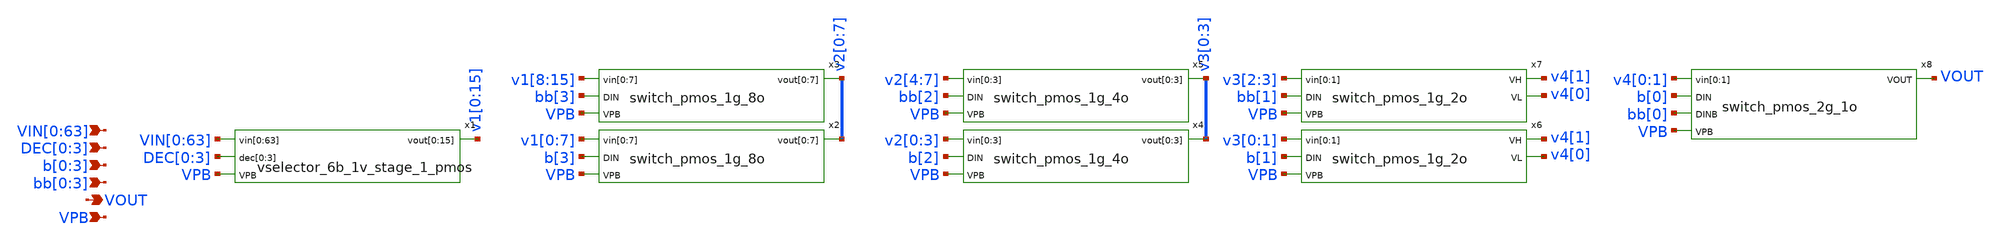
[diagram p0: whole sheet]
** sch_path: xschem/vselector_6b_1v_pmos.sch
**.subckt vselector_6b_1v_pmos
*+ VIN[0],VIN[1],VIN[2],VIN[3],VIN[4],VIN[5],VIN[6],VIN[7],VIN[8],VIN[9],VIN[10],VIN[11],VIN[12],VIN[13],VIN[14],VIN[15],VIN[16],VIN[17],VIN[18],VIN[19],VIN[20],VIN[21],VIN[22],VIN[23],VIN[24],VIN[25],VIN[26],VIN[27],VIN[28],VIN[29],VIN[30],VIN[31],VIN[32],VIN[33],VIN[34],VIN[35],VIN[36],VIN[37],VIN[38],VIN[39],VIN[40],VIN[41],VIN[42],VIN[43],VIN[44],VIN[45],VIN[46],VIN[47],VIN[48],VIN[49],VIN[50],VIN[51],VIN[52],VIN[53],VIN[54],VIN[55],VIN[56],VIN[57],VIN[58],VIN[59],VIN[60],VIN[61],VIN[62],VIN[63] VOUT VPB DEC[0],DEC[1],DEC[2],DEC[3] b[0],b[1],b[2],b[3] bb[0],bb[1],bb[2],bb[3]
*.ipin
*+ VIN[0],VIN[1],VIN[2],VIN[3],VIN[4],VIN[5],VIN[6],VIN[7],VIN[8],VIN[9],VIN[10],VIN[11],VIN[12],VIN[13],VIN[14],VIN[15],VIN[16],VIN[17],VIN[18],VIN[19],VIN[20],VIN[21],VIN[22],VIN[23],VIN[24],VIN[25],VIN[26],VIN[27],VIN[28],VIN[29],VIN[30],VIN[31],VIN[32],VIN[33],VIN[34],VIN[35],VIN[36],VIN[37],VIN[38],VIN[39],VIN[40],VIN[41],VIN[42],VIN[43],VIN[44],VIN[45],VIN[46],VIN[47],VIN[48],VIN[49],VIN[50],VIN[51],VIN[52],VIN[53],VIN[54],VIN[55],VIN[56],VIN[57],VIN[58],VIN[59],VIN[60],VIN[61],VIN[62],VIN[63]
*.opin VOUT
*.ipin VPB
*.ipin DEC[0],DEC[1],DEC[2],DEC[3]
*.ipin b[0],b[1],b[2],b[3]
*.ipin bb[0],bb[1],bb[2],bb[3]
x1 VIN[0] VIN[1] VIN[2] VIN[3] VIN[4] VIN[5] VIN[6] VIN[7] VIN[8] VIN[9] VIN[10] VIN[11] VIN[12]
+ VIN[13] VIN[14] VIN[15] VIN[16] VIN[17] VIN[18] VIN[19] VIN[20] VIN[21] VIN[22] VIN[23] VIN[24] VIN[25]
+ VIN[26] VIN[27] VIN[28] VIN[29] VIN[30] VIN[31] VIN[32] VIN[33] VIN[34] VIN[35] VIN[36] VIN[37] VIN[38]
+ VIN[39] VIN[40] VIN[41] VIN[42] VIN[43] VIN[44] VIN[45] VIN[46] VIN[47] VIN[48] VIN[49] VIN[50] VIN[51]
+ VIN[52] VIN[53] VIN[54] VIN[55] VIN[56] VIN[57] VIN[58] VIN[59] VIN[60] VIN[61] VIN[62] VIN[63] DEC[0]
+ DEC[1] DEC[2] DEC[3] v1[0] v1[1] v1[2] v1[3] v1[4] v1[5] v1[6] v1[7] v1[8] v1[9] v1[10] v1[11] v1[12]
+ v1[13] v1[14] v1[15] VPB vselector_6b_1v_stage_1_pmos
x2 v1[0] v1[1] v1[2] v1[3] v1[4] v1[5] v1[6] v1[7] b[3] v2[0] v2[1] v2[2] v2[3] v2[4] v2[5] v2[6]
+ v2[7] VPB switch_pmos_1g_8o
x3 v1[8] v1[9] v1[10] v1[11] v1[12] v1[13] v1[14] v1[15] bb[3] v2[0] v2[1] v2[2] v2[3] v2[4] v2[5]
+ v2[6] v2[7] VPB switch_pmos_1g_8o
x4 v2[0] v2[1] v2[2] v2[3] b[2] v3[0] v3[1] v3[2] v3[3] VPB switch_pmos_1g_4o
x5 v2[4] v2[5] v2[6] v2[7] bb[2] v3[0] v3[1] v3[2] v3[3] VPB switch_pmos_1g_4o
x6 v3[0] v3[1] b[1] v4[1] v4[0] VPB switch_pmos_1g_2o
x7 v3[2] v3[3] bb[1] v4[1] v4[0] VPB switch_pmos_1g_2o
x8 v4[0] v4[1] b[0] bb[0] VOUT VPB switch_pmos_2g_1o
**.ends

* expanding   symbol:  vselector_6b_1v_stage_1_pmos.sym # of pins=4
** sym_path: xschem/vselector_6b_1v_stage_1_pmos.sym
** sch_path: xschem/vselector_6b_1v_stage_1_pmos.sch
.subckt vselector_6b_1v_stage_1_pmos vin[0] vin[1] vin[2] vin[3] vin[4] vin[5] vin[6] vin[7] vin[8]
+ vin[9] vin[10] vin[11] vin[12] vin[13] vin[14] vin[15] vin[16] vin[17] vin[18] vin[19] vin[20] vin[21]
+ vin[22] vin[23] vin[24] vin[25] vin[26] vin[27] vin[28] vin[29] vin[30] vin[31] vin[32] vin[33] vin[34]
+ vin[35] vin[36] vin[37] vin[38] vin[39] vin[40] vin[41] vin[42] vin[43] vin[44] vin[45] vin[46] vin[47]
+ vin[48] vin[49] vin[50] vin[51] vin[52] vin[53] vin[54] vin[55] vin[56] vin[57] vin[58] vin[59] vin[60]
+ vin[61] vin[62] vin[63] dec[0] dec[1] dec[2] dec[3] vout[0] vout[1] vout[2] vout[3] vout[4] vout[5] vout[6]
+ vout[7] vout[8] vout[9] vout[10] vout[11] vout[12] vout[13] vout[14] vout[15] VPB
*.ipin
*+ vin[0],vin[1],vin[2],vin[3],vin[4],vin[5],vin[6],vin[7],vin[8],vin[9],vin[10],vin[11],vin[12],vin[13],vin[14],vin[15],vin[16],vin[17],vin[18],vin[19],vin[20],vin[21],vin[22],vin[23],vin[24],vin[25],vin[26],vin[27],vin[28],vin[29],vin[30],vin[31],vin[32],vin[33],vin[34],vin[35],vin[36],vin[37],vin[38],vin[39],vin[40],vin[41],vin[42],vin[43],vin[44],vin[45],vin[46],vin[47],vin[48],vin[49],vin[50],vin[51],vin[52],vin[53],vin[54],vin[55],vin[56],vin[57],vin[58],vin[59],vin[60],vin[61],vin[62],vin[63]
*.opin
*+ vout[0],vout[1],vout[2],vout[3],vout[4],vout[5],vout[6],vout[7],vout[8],vout[9],vout[10],vout[11],vout[12],vout[13],vout[14],vout[15]
*.ipin VPB
*.ipin dec[0],dec[1],dec[2],dec[3]
x1 vin[0] vin[1] vin[2] vin[3] vin[4] vin[5] vin[6] vin[7] vin[8] vin[9] vin[10] vin[11] vin[12]
+ vin[13] vin[14] vin[15] dec[0] vout[0] vout[1] vout[2] vout[3] vout[4] vout[5] vout[6] vout[7] vout[8]
+ vout[9] vout[10] vout[11] vout[12] vout[13] vout[14] vout[15] VPB vselector_16b_1v_pmos
x2 vin[16] vin[17] vin[18] vin[19] vin[20] vin[21] vin[22] vin[23] vin[24] vin[25] vin[26] vin[27]
+ vin[28] vin[29] vin[30] vin[31] dec[1] vout[0] vout[1] vout[2] vout[3] vout[4] vout[5] vout[6] vout[7]
+ vout[8] vout[9] vout[10] vout[11] vout[12] vout[13] vout[14] vout[15] VPB vselector_16b_1v_pmos
x3 vin[32] vin[33] vin[34] vin[35] vin[36] vin[37] vin[38] vin[39] vin[40] vin[41] vin[42] vin[43]
+ vin[44] vin[45] vin[46] vin[47] dec[2] vout[0] vout[1] vout[2] vout[3] vout[4] vout[5] vout[6] vout[7]
+ vout[8] vout[9] vout[10] vout[11] vout[12] vout[13] vout[14] vout[15] VPB vselector_16b_1v_pmos
x4 vin[48] vin[49] vin[50] vin[51] vin[52] vin[53] vin[54] vin[55] vin[56] vin[57] vin[58] vin[59]
+ vin[60] vin[61] vin[62] vin[63] dec[3] vout[0] vout[1] vout[2] vout[3] vout[4] vout[5] vout[6] vout[7]
+ vout[8] vout[9] vout[10] vout[11] vout[12] vout[13] vout[14] vout[15] VPB vselector_16b_1v_pmos
.ends


* expanding   symbol:  switch_pmos_1g_8o.sym # of pins=4
** sym_path: xschem/switch_pmos_1g_8o.sym
** sch_path: xschem/switch_pmos_1g_8o.sch
.subckt switch_pmos_1g_8o vin[0] vin[1] vin[2] vin[3] vin[4] vin[5] vin[6] vin[7] DIN vout[0]
+ vout[1] vout[2] vout[3] vout[4] vout[5] vout[6] vout[7] VPB
*.ipin vin[0],vin[1],vin[2],vin[3],vin[4],vin[5],vin[6],vin[7]
*.opin vout[0],vout[1],vout[2],vout[3],vout[4],vout[5],vout[6],vout[7]
*.ipin VPB
*.ipin DIN
.param wp=0.42 wn=0.42 l=0.5

XM1 vout[0] DIN vin[0] VPB sky130_fd_pr__pfet_g5v0d10v5 L=l W=wp nf=1 ad='int((nf+1)/2) * W/nf * 0.29'
+ as='int((nf+2)/2) * W/nf * 0.29' pd='2*int((nf+1)/2) * (W/nf + 0.29)' ps='2*int((nf+2)/2) * (W/nf + 0.29)'
+ nrd='0.29 / W' nrs='0.29 / W' sa=0 sb=0 sd=0 mult=1 m=1
XM2 vout[1] DIN vin[1] VPB sky130_fd_pr__pfet_g5v0d10v5 L=l W=wp nf=1 ad='int((nf+1)/2) * W/nf * 0.29'
+ as='int((nf+2)/2) * W/nf * 0.29' pd='2*int((nf+1)/2) * (W/nf + 0.29)' ps='2*int((nf+2)/2) * (W/nf + 0.29)'
+ nrd='0.29 / W' nrs='0.29 / W' sa=0 sb=0 sd=0 mult=1 m=1
XM3 vout[2] DIN vin[2] VPB sky130_fd_pr__pfet_g5v0d10v5 L=l W=wp nf=1 ad='int((nf+1)/2) * W/nf * 0.29'
+ as='int((nf+2)/2) * W/nf * 0.29' pd='2*int((nf+1)/2) * (W/nf + 0.29)' ps='2*int((nf+2)/2) * (W/nf + 0.29)'
+ nrd='0.29 / W' nrs='0.29 / W' sa=0 sb=0 sd=0 mult=1 m=1
XM4 vout[3] DIN vin[3] VPB sky130_fd_pr__pfet_g5v0d10v5 L=l W=wp nf=1 ad='int((nf+1)/2) * W/nf * 0.29'
+ as='int((nf+2)/2) * W/nf * 0.29' pd='2*int((nf+1)/2) * (W/nf + 0.29)' ps='2*int((nf+2)/2) * (W/nf + 0.29)'
+ nrd='0.29 / W' nrs='0.29 / W' sa=0 sb=0 sd=0 mult=1 m=1
XM5 vout[4] DIN vin[4] VPB sky130_fd_pr__pfet_g5v0d10v5 L=l W=wp nf=1 ad='int((nf+1)/2) * W/nf * 0.29'
+ as='int((nf+2)/2) * W/nf * 0.29' pd='2*int((nf+1)/2) * (W/nf + 0.29)' ps='2*int((nf+2)/2) * (W/nf + 0.29)'
+ nrd='0.29 / W' nrs='0.29 / W' sa=0 sb=0 sd=0 mult=1 m=1
XM6 vout[5] DIN vin[5] VPB sky130_fd_pr__pfet_g5v0d10v5 L=l W=wp nf=1 ad='int((nf+1)/2) * W/nf * 0.29'
+ as='int((nf+2)/2) * W/nf * 0.29' pd='2*int((nf+1)/2) * (W/nf + 0.29)' ps='2*int((nf+2)/2) * (W/nf + 0.29)'
+ nrd='0.29 / W' nrs='0.29 / W' sa=0 sb=0 sd=0 mult=1 m=1
XM7 vout[6] DIN vin[6] VPB sky130_fd_pr__pfet_g5v0d10v5 L=l W=wp nf=1 ad='int((nf+1)/2) * W/nf * 0.29'
+ as='int((nf+2)/2) * W/nf * 0.29' pd='2*int((nf+1)/2) * (W/nf + 0.29)' ps='2*int((nf+2)/2) * (W/nf + 0.29)'
+ nrd='0.29 / W' nrs='0.29 / W' sa=0 sb=0 sd=0 mult=1 m=1
XM8 vout[7] DIN vin[7] VPB sky130_fd_pr__pfet_g5v0d10v5 L=l W=wp nf=1 ad='int((nf+1)/2) * W/nf * 0.29'
+ as='int((nf+2)/2) * W/nf * 0.29' pd='2*int((nf+1)/2) * (W/nf + 0.29)' ps='2*int((nf+2)/2) * (W/nf + 0.29)'
+ nrd='0.29 / W' nrs='0.29 / W' sa=0 sb=0 sd=0 mult=1 m=1
.ends


* expanding   symbol:  switch_pmos_1g_4o.sym # of pins=4
** sym_path: xschem/switch_pmos_1g_4o.sym
** sch_path: xschem/switch_pmos_1g_4o.sch
.subckt switch_pmos_1g_4o vin[0] vin[1] vin[2] vin[3] DIN vout[0] vout[1] vout[2] vout[3] VPB
*.ipin vin[0],vin[1],vin[2],vin[3]
*.opin vout[0],vout[1],vout[2],vout[3]
*.ipin VPB
*.ipin DIN
.param wp=0.42 wn=0.42 l=0.5

XM1 vout[0] DIN vin[0] VPB sky130_fd_pr__pfet_g5v0d10v5 L=l W=wp nf=1 ad='int((nf+1)/2) * W/nf * 0.29'
+ as='int((nf+2)/2) * W/nf * 0.29' pd='2*int((nf+1)/2) * (W/nf + 0.29)' ps='2*int((nf+2)/2) * (W/nf + 0.29)'
+ nrd='0.29 / W' nrs='0.29 / W' sa=0 sb=0 sd=0 mult=1 m=1
XM2 vout[1] DIN vin[1] VPB sky130_fd_pr__pfet_g5v0d10v5 L=l W=wp nf=1 ad='int((nf+1)/2) * W/nf * 0.29'
+ as='int((nf+2)/2) * W/nf * 0.29' pd='2*int((nf+1)/2) * (W/nf + 0.29)' ps='2*int((nf+2)/2) * (W/nf + 0.29)'
+ nrd='0.29 / W' nrs='0.29 / W' sa=0 sb=0 sd=0 mult=1 m=1
XM3 vout[2] DIN vin[2] VPB sky130_fd_pr__pfet_g5v0d10v5 L=l W=wp nf=1 ad='int((nf+1)/2) * W/nf * 0.29'
+ as='int((nf+2)/2) * W/nf * 0.29' pd='2*int((nf+1)/2) * (W/nf + 0.29)' ps='2*int((nf+2)/2) * (W/nf + 0.29)'
+ nrd='0.29 / W' nrs='0.29 / W' sa=0 sb=0 sd=0 mult=1 m=1
XM4 vout[3] DIN vin[3] VPB sky130_fd_pr__pfet_g5v0d10v5 L=l W=wp nf=1 ad='int((nf+1)/2) * W/nf * 0.29'
+ as='int((nf+2)/2) * W/nf * 0.29' pd='2*int((nf+1)/2) * (W/nf + 0.29)' ps='2*int((nf+2)/2) * (W/nf + 0.29)'
+ nrd='0.29 / W' nrs='0.29 / W' sa=0 sb=0 sd=0 mult=1 m=1
.ends


* expanding   symbol:  switch_pmos_1g_2o.sym # of pins=5
** sym_path: xschem/switch_pmos_1g_2o.sym
** sch_path: xschem/switch_pmos_1g_2o.sch
.subckt switch_pmos_1g_2o vin[0] vin[1] DIN VH VL VPB
*.ipin vin[0],vin[1]
*.opin VH
*.ipin VPB
*.ipin DIN
*.opin VL
.param wp=0.42 wn=0.42 l=0.5

XM1 VL DIN vin[0] VPB sky130_fd_pr__pfet_g5v0d10v5 L=l W=wp nf=1 ad='int((nf+1)/2) * W/nf * 0.29' as='int((nf+2)/2) * W/nf * 0.29'
+ pd='2*int((nf+1)/2) * (W/nf + 0.29)' ps='2*int((nf+2)/2) * (W/nf + 0.29)' nrd='0.29 / W' nrs='0.29 / W'
+ sa=0 sb=0 sd=0 mult=1 m=1
XM2 VH DIN vin[1] VPB sky130_fd_pr__pfet_g5v0d10v5 L=l W=wp nf=1 ad='int((nf+1)/2) * W/nf * 0.29' as='int((nf+2)/2) * W/nf * 0.29'
+ pd='2*int((nf+1)/2) * (W/nf + 0.29)' ps='2*int((nf+2)/2) * (W/nf + 0.29)' nrd='0.29 / W' nrs='0.29 / W'
+ sa=0 sb=0 sd=0 mult=1 m=1
.ends


* expanding   symbol:  switch_pmos_2g_1o.sym # of pins=5
** sym_path: xschem/switch_pmos_2g_1o.sym
** sch_path: xschem/switch_pmos_2g_1o.sch
.subckt switch_pmos_2g_1o vin[0] vin[1] DIN DINB VOUT VPB
*.ipin vin[0],vin[1]
*.opin VOUT
*.ipin VPB
*.ipin DIN
*.ipin DINB
.param wp=0.42 wn=0.42 l=0.5

XM1 VOUT DIN vin[0] VPB sky130_fd_pr__pfet_g5v0d10v5 L=l W=wp nf=1 ad='int((nf+1)/2) * W/nf * 0.29' as='int((nf+2)/2) * W/nf * 0.29'
+ pd='2*int((nf+1)/2) * (W/nf + 0.29)' ps='2*int((nf+2)/2) * (W/nf + 0.29)' nrd='0.29 / W' nrs='0.29 / W'
+ sa=0 sb=0 sd=0 mult=1 m=1
XM2 VOUT DINB vin[1] VPB sky130_fd_pr__pfet_g5v0d10v5 L=l W=wp nf=1 ad='int((nf+1)/2) * W/nf * 0.29'
+ as='int((nf+2)/2) * W/nf * 0.29' pd='2*int((nf+1)/2) * (W/nf + 0.29)' ps='2*int((nf+2)/2) * (W/nf + 0.29)'
+ nrd='0.29 / W' nrs='0.29 / W' sa=0 sb=0 sd=0 mult=1 m=1
.ends


* expanding   symbol:  vselector_16b_1v_pmos.sym # of pins=4
** sym_path: xschem/vselector_16b_1v_pmos.sym
** sch_path: xschem/vselector_16b_1v_pmos.sch
.subckt vselector_16b_1v_pmos vin[0] vin[1] vin[2] vin[3] vin[4] vin[5] vin[6] vin[7] vin[8] vin[9]
+ vin[10] vin[11] vin[12] vin[13] vin[14] vin[15] DIN vout[0] vout[1] vout[2] vout[3] vout[4] vout[5] vout[6]
+ vout[7] vout[8] vout[9] vout[10] vout[11] vout[12] vout[13] vout[14] vout[15] VPB
*.ipin
*+ vin[0],vin[1],vin[2],vin[3],vin[4],vin[5],vin[6],vin[7],vin[8],vin[9],vin[10],vin[11],vin[12],vin[13],vin[14],vin[15]
*.opin
*+ vout[0],vout[1],vout[2],vout[3],vout[4],vout[5],vout[6],vout[7],vout[8],vout[9],vout[10],vout[11],vout[12],vout[13],vout[14],vout[15]
*.ipin VPB
*.ipin DIN
.param wp=0.42 wn=0.42 l=0.5

XM1 vout[0] DIN vin[0] VPB sky130_fd_pr__pfet_g5v0d10v5 L=l W=wp nf=1 ad='int((nf+1)/2) * W/nf * 0.29'
+ as='int((nf+2)/2) * W/nf * 0.29' pd='2*int((nf+1)/2) * (W/nf + 0.29)' ps='2*int((nf+2)/2) * (W/nf + 0.29)'
+ nrd='0.29 / W' nrs='0.29 / W' sa=0 sb=0 sd=0 mult=1 m=1
XM2 vout[1] DIN vin[1] VPB sky130_fd_pr__pfet_g5v0d10v5 L=l W=wp nf=1 ad='int((nf+1)/2) * W/nf * 0.29'
+ as='int((nf+2)/2) * W/nf * 0.29' pd='2*int((nf+1)/2) * (W/nf + 0.29)' ps='2*int((nf+2)/2) * (W/nf + 0.29)'
+ nrd='0.29 / W' nrs='0.29 / W' sa=0 sb=0 sd=0 mult=1 m=1
XM3 vout[2] DIN vin[2] VPB sky130_fd_pr__pfet_g5v0d10v5 L=l W=wp nf=1 ad='int((nf+1)/2) * W/nf * 0.29'
+ as='int((nf+2)/2) * W/nf * 0.29' pd='2*int((nf+1)/2) * (W/nf + 0.29)' ps='2*int((nf+2)/2) * (W/nf + 0.29)'
+ nrd='0.29 / W' nrs='0.29 / W' sa=0 sb=0 sd=0 mult=1 m=1
XM4 vout[3] DIN vin[3] VPB sky130_fd_pr__pfet_g5v0d10v5 L=l W=wp nf=1 ad='int((nf+1)/2) * W/nf * 0.29'
+ as='int((nf+2)/2) * W/nf * 0.29' pd='2*int((nf+1)/2) * (W/nf + 0.29)' ps='2*int((nf+2)/2) * (W/nf + 0.29)'
+ nrd='0.29 / W' nrs='0.29 / W' sa=0 sb=0 sd=0 mult=1 m=1
XM5 vout[4] DIN vin[4] VPB sky130_fd_pr__pfet_g5v0d10v5 L=l W=wp nf=1 ad='int((nf+1)/2) * W/nf * 0.29'
+ as='int((nf+2)/2) * W/nf * 0.29' pd='2*int((nf+1)/2) * (W/nf + 0.29)' ps='2*int((nf+2)/2) * (W/nf + 0.29)'
+ nrd='0.29 / W' nrs='0.29 / W' sa=0 sb=0 sd=0 mult=1 m=1
XM6 vout[5] DIN vin[5] VPB sky130_fd_pr__pfet_g5v0d10v5 L=l W=wp nf=1 ad='int((nf+1)/2) * W/nf * 0.29'
+ as='int((nf+2)/2) * W/nf * 0.29' pd='2*int((nf+1)/2) * (W/nf + 0.29)' ps='2*int((nf+2)/2) * (W/nf + 0.29)'
+ nrd='0.29 / W' nrs='0.29 / W' sa=0 sb=0 sd=0 mult=1 m=1
XM7 vout[6] DIN vin[6] VPB sky130_fd_pr__pfet_g5v0d10v5 L=l W=wp nf=1 ad='int((nf+1)/2) * W/nf * 0.29'
+ as='int((nf+2)/2) * W/nf * 0.29' pd='2*int((nf+1)/2) * (W/nf + 0.29)' ps='2*int((nf+2)/2) * (W/nf + 0.29)'
+ nrd='0.29 / W' nrs='0.29 / W' sa=0 sb=0 sd=0 mult=1 m=1
XM8 vout[7] DIN vin[7] VPB sky130_fd_pr__pfet_g5v0d10v5 L=l W=wp nf=1 ad='int((nf+1)/2) * W/nf * 0.29'
+ as='int((nf+2)/2) * W/nf * 0.29' pd='2*int((nf+1)/2) * (W/nf + 0.29)' ps='2*int((nf+2)/2) * (W/nf + 0.29)'
+ nrd='0.29 / W' nrs='0.29 / W' sa=0 sb=0 sd=0 mult=1 m=1
XM9 vout[8] DIN vin[8] VPB sky130_fd_pr__pfet_g5v0d10v5 L=l W=wp nf=1 ad='int((nf+1)/2) * W/nf * 0.29'
+ as='int((nf+2)/2) * W/nf * 0.29' pd='2*int((nf+1)/2) * (W/nf + 0.29)' ps='2*int((nf+2)/2) * (W/nf + 0.29)'
+ nrd='0.29 / W' nrs='0.29 / W' sa=0 sb=0 sd=0 mult=1 m=1
XM10 vout[9] DIN vin[9] VPB sky130_fd_pr__pfet_g5v0d10v5 L=l W=wp nf=1 ad='int((nf+1)/2) * W/nf * 0.29'
+ as='int((nf+2)/2) * W/nf * 0.29' pd='2*int((nf+1)/2) * (W/nf + 0.29)' ps='2*int((nf+2)/2) * (W/nf + 0.29)'
+ nrd='0.29 / W' nrs='0.29 / W' sa=0 sb=0 sd=0 mult=1 m=1
XM11 vout[10] DIN vin[10] VPB sky130_fd_pr__pfet_g5v0d10v5 L=l W=wp nf=1 ad='int((nf+1)/2) * W/nf * 0.29'
+ as='int((nf+2)/2) * W/nf * 0.29' pd='2*int((nf+1)/2) * (W/nf + 0.29)' ps='2*int((nf+2)/2) * (W/nf + 0.29)'
+ nrd='0.29 / W' nrs='0.29 / W' sa=0 sb=0 sd=0 mult=1 m=1
XM12 vout[11] DIN vin[11] VPB sky130_fd_pr__pfet_g5v0d10v5 L=l W=wp nf=1 ad='int((nf+1)/2) * W/nf * 0.29'
+ as='int((nf+2)/2) * W/nf * 0.29' pd='2*int((nf+1)/2) * (W/nf + 0.29)' ps='2*int((nf+2)/2) * (W/nf + 0.29)'
+ nrd='0.29 / W' nrs='0.29 / W' sa=0 sb=0 sd=0 mult=1 m=1
XM13 vout[12] DIN vin[12] VPB sky130_fd_pr__pfet_g5v0d10v5 L=l W=wp nf=1 ad='int((nf+1)/2) * W/nf * 0.29'
+ as='int((nf+2)/2) * W/nf * 0.29' pd='2*int((nf+1)/2) * (W/nf + 0.29)' ps='2*int((nf+2)/2) * (W/nf + 0.29)'
+ nrd='0.29 / W' nrs='0.29 / W' sa=0 sb=0 sd=0 mult=1 m=1
XM14 vout[13] DIN vin[13] VPB sky130_fd_pr__pfet_g5v0d10v5 L=l W=wp nf=1 ad='int((nf+1)/2) * W/nf * 0.29'
+ as='int((nf+2)/2) * W/nf * 0.29' pd='2*int((nf+1)/2) * (W/nf + 0.29)' ps='2*int((nf+2)/2) * (W/nf + 0.29)'
+ nrd='0.29 / W' nrs='0.29 / W' sa=0 sb=0 sd=0 mult=1 m=1
XM15 vout[14] DIN vin[14] VPB sky130_fd_pr__pfet_g5v0d10v5 L=l W=wp nf=1 ad='int((nf+1)/2) * W/nf * 0.29'
+ as='int((nf+2)/2) * W/nf * 0.29' pd='2*int((nf+1)/2) * (W/nf + 0.29)' ps='2*int((nf+2)/2) * (W/nf + 0.29)'
+ nrd='0.29 / W' nrs='0.29 / W' sa=0 sb=0 sd=0 mult=1 m=1
XM16 vout[15] DIN vin[15] VPB sky130_fd_pr__pfet_g5v0d10v5 L=l W=wp nf=1 ad='int((nf+1)/2) * W/nf * 0.29'
+ as='int((nf+2)/2) * W/nf * 0.29' pd='2*int((nf+1)/2) * (W/nf + 0.29)' ps='2*int((nf+2)/2) * (W/nf + 0.29)'
+ nrd='0.29 / W' nrs='0.29 / W' sa=0 sb=0 sd=0 mult=1 m=1
.ends

.end
